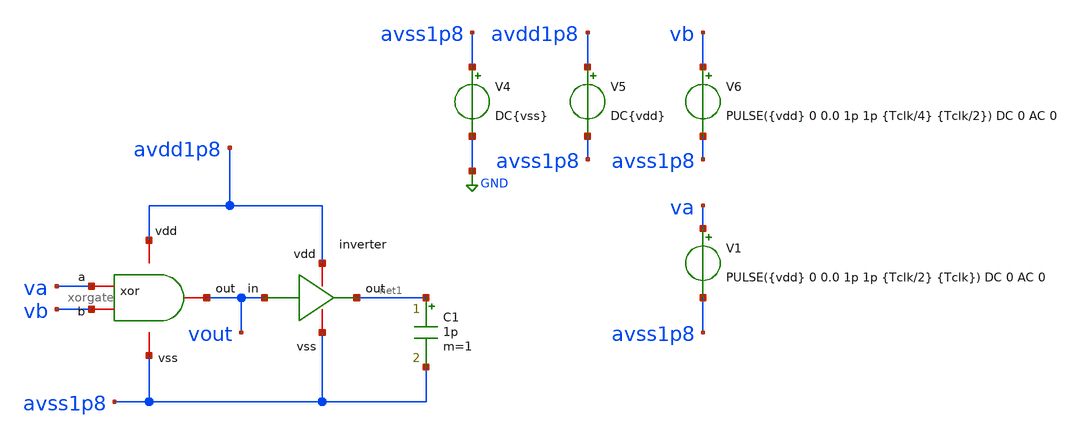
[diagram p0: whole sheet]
** sch_path: verification/testbenches/tb_xorgate.sch
**.subckt tb_xorgate
C1 net1 avss1p8 1p m=1
V4 avss1p8 GND DC{vss}
V5 avdd1p8 avss1p8 DC{vdd}
V6 vb avss1p8 PULSE({vdd} 0 0.0 1p 1p {Tclk/4} {Tclk/2}) DC 0 AC 0
x2 avdd1p8 net1 vout avss1p8 inverter
V1 va avss1p8 PULSE({vdd} 0 0.0 1p 1p {Tclk/2} {Tclk}) DC 0 AC 0
x1 va avdd1p8 vb avss1p8 vout xorgate
**** begin user architecture code


* Circuit Parameters
.param vdd = 1.2
.param vss = 0.0
.param Tclk = 10n
.options TEMP = 27.0
* Include Models - IHP SG13G2
.lib cornerMOSlv.lib mos_tt
* OP Parameters & Singals to save
.save all
*Simulations
.control
tran 0.01u 100n
setplot tran1
plot v(va) v(vb) + 1.2 v(vout) + 2.4
set filetype = ascii
write dcsweep.raw
.endc
.end


**** end user architecture code
**.ends

* expanding   symbol:  blocks/inverter/schematic/inverter.sym # of pins=4
** sym_path: design/blocks/inverter/schematic/inverter.sym
** sch_path: design/blocks/inverter/schematic/inverter.sch
.subckt inverter vdd out in vss
*.iopin vdd
*.iopin out
*.iopin vss
*.iopin in
XM1 out in vss vss sky130_fd_pr__nfet_01v8 L=0.15 W=0.75 nf=1 ad='int((nf+1)/2) * W/nf * 0.29' as='int((nf+2)/2) * W/nf * 0.29'
+ pd='2*int((nf+1)/2) * (W/nf + 0.29)' ps='2*int((nf+2)/2) * (W/nf + 0.29)' nrd='0.29 / W' nrs='0.29 / W'
+ sa=0 sb=0 sd=0 mult=1 m=1
XM2 out in vdd vdd sky130_fd_pr__pfet_01v8 L=0.15 W=1.5 nf=1 ad='int((nf+1)/2) * W/nf * 0.29' as='int((nf+2)/2) * W/nf * 0.29'
+ pd='2*int((nf+1)/2) * (W/nf + 0.29)' ps='2*int((nf+2)/2) * (W/nf + 0.29)' nrd='0.29 / W' nrs='0.29 / W'
+ sa=0 sb=0 sd=0 mult=1 m=1
.ends


* expanding   symbol:  blocks/xorgate/schematic/xorgate.sym # of pins=5
** sym_path: design/blocks/xorgate/schematic/xorgate.sym
** sch_path: design/blocks/xorgate/schematic/xorgate.sch
.subckt xorgate a vdd b vss out
*.iopin a
*.iopin b
*.iopin vdd
*.iopin vss
*.iopin out
XM3 out a net1 vdd sg13_lv_pmos w=1.5u l=0.15u ng=1 m=1 mm_ok=1
XM1 out b net1 vdd sg13_lv_pmos w=1.5u l=0.15u ng=1 m=1 mm_ok=1
XM4 out na net2 vss sg13_lv_nmos w=1.5u l=0.15u ng=1 m=1 mm_ok=1
x1 vdd nb b vss inverter
x2 vdd na a vss inverter
XM2 net1 nb vdd vdd sg13_lv_pmos w=1.5u l=0.15u ng=1 m=1 mm_ok=1
XM5 net1 na vdd vdd sg13_lv_pmos w=1.5u l=0.15u ng=1 m=1 mm_ok=1
XM7 out a net3 vss sg13_lv_nmos w=1.5u l=0.15u ng=1 m=1 mm_ok=1
XM8 net2 nb vss vss sg13_lv_nmos w=1.5u l=0.15u ng=1 m=1 mm_ok=1
XM9 net3 b vss vss sg13_lv_nmos w=1.5u l=0.15u ng=1 m=1 mm_ok=1
.ends

.GLOBAL GND
.end
